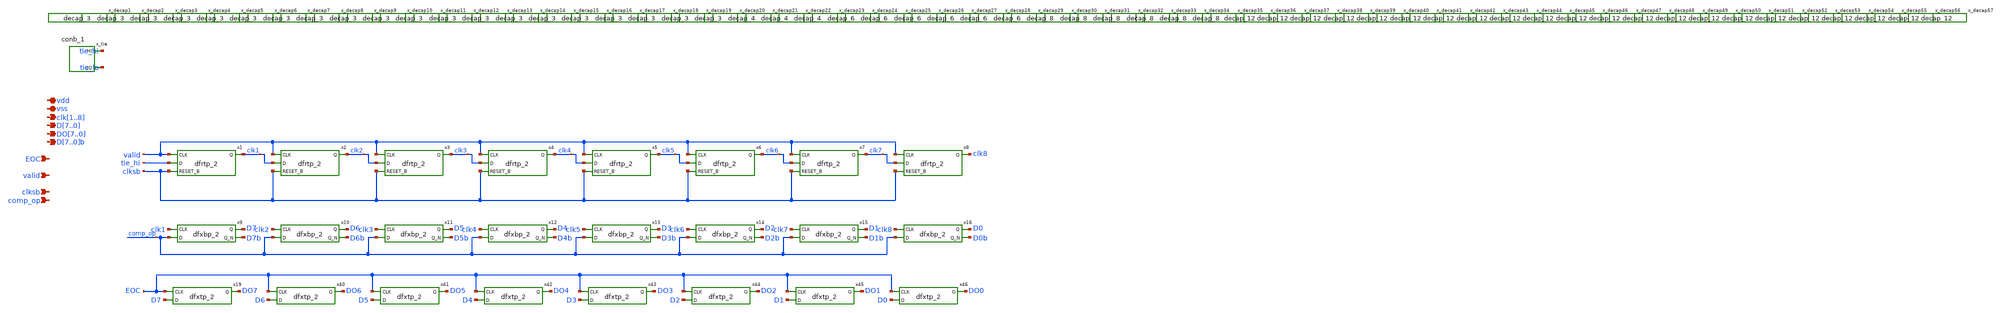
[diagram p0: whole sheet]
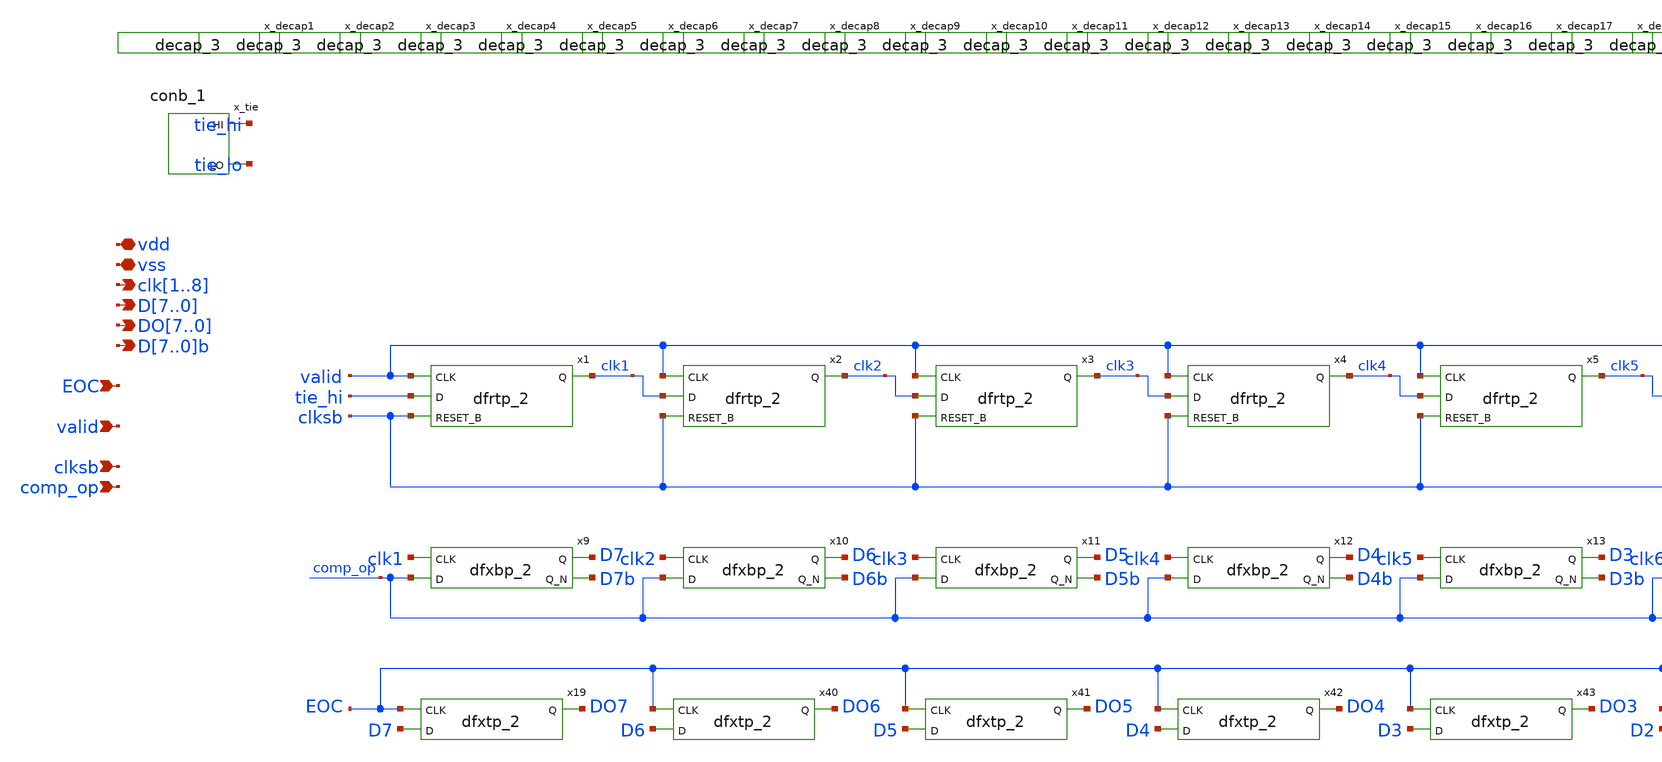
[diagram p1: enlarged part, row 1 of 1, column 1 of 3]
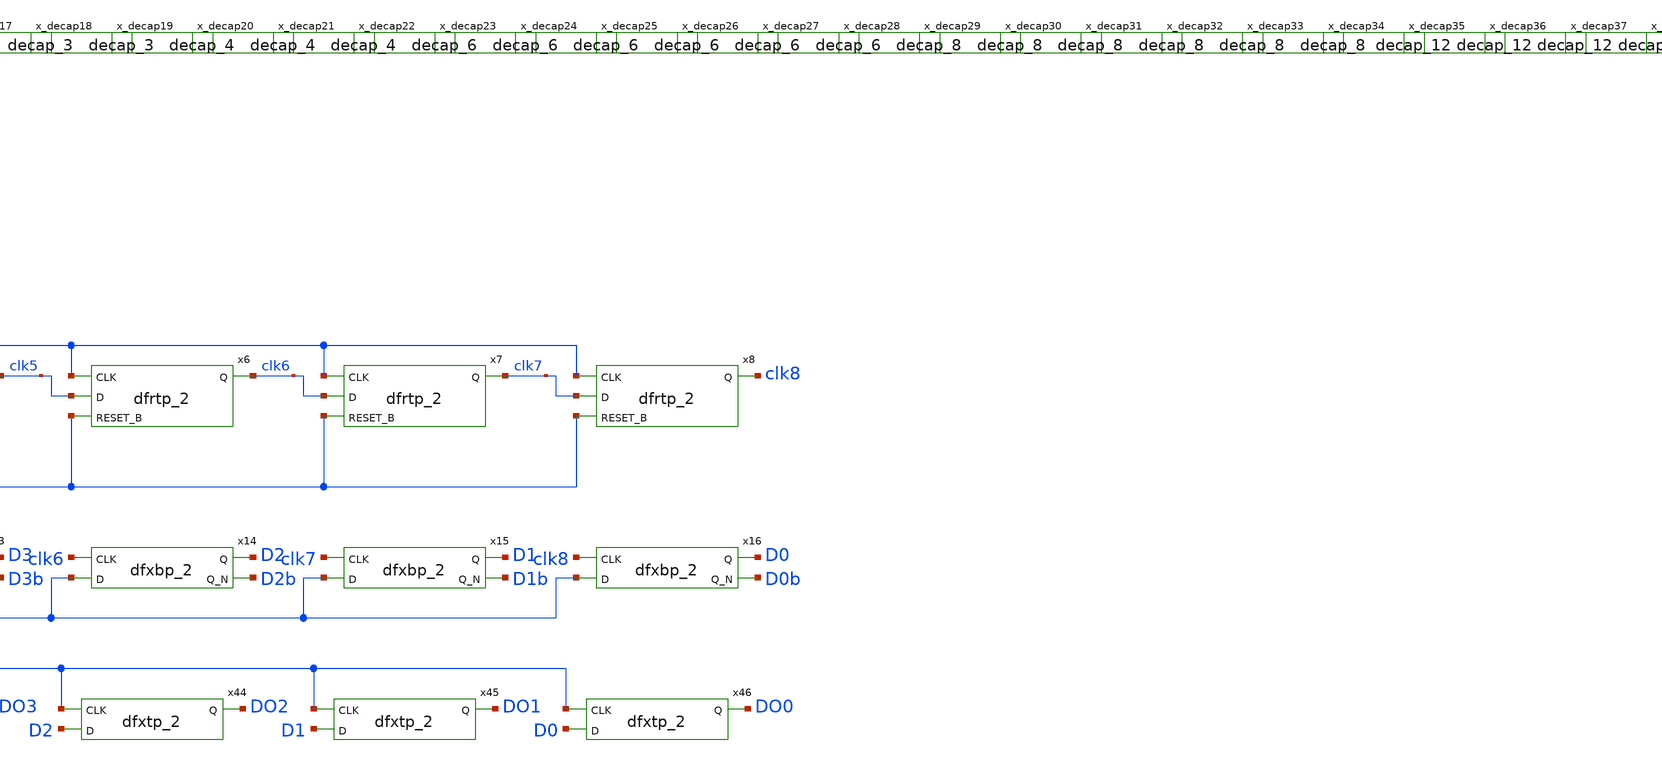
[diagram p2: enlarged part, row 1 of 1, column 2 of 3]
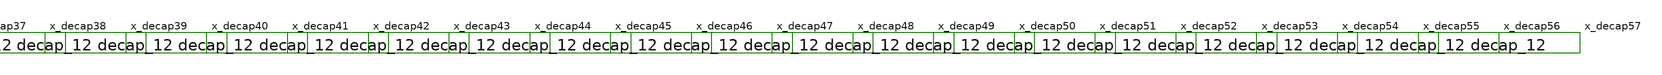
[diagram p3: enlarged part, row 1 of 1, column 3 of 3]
** sch_path: xschem/sar-adc/sarlogic.sch
**.subckt sarlogic valid comp_op D7,D6,D5,D4,D3,D2,D1,D0 vdd vss D7b,D6b,D5b,D4b,D3b,D2b,D1b,D0b
*+ clk1,clk2,clk3,clk4,clk5,clk6,clk7,clk8 DO7,DO6,DO5,DO4,DO3,DO2,DO1,DO0 clksb EOC
*.ipin valid
*.ipin comp_op
*.opin D7,D6,D5,D4,D3,D2,D1,D0
*.iopin vdd
*.iopin vss
*.opin D7b,D6b,D5b,D4b,D3b,D2b,D1b,D0b
*.opin clk1,clk2,clk3,clk4,clk5,clk6,clk7,clk8
*.opin DO7,DO6,DO5,DO4,DO3,DO2,DO1,DO0
*.ipin clksb
*.ipin EOC
x1 valid tie_hi clksb vss vss vdd vdd clk1 sky130_fd_sc_hd__dfrtp_2
x2 valid clk1 clksb vss vss vdd vdd clk2 sky130_fd_sc_hd__dfrtp_2
x3 valid clk2 clksb vss vss vdd vdd clk3 sky130_fd_sc_hd__dfrtp_2
x4 valid clk3 clksb vss vss vdd vdd clk4 sky130_fd_sc_hd__dfrtp_2
x5 valid clk4 clksb vss vss vdd vdd clk5 sky130_fd_sc_hd__dfrtp_2
x6 valid clk5 clksb vss vss vdd vdd clk6 sky130_fd_sc_hd__dfrtp_2
x7 valid clk6 clksb vss vss vdd vdd clk7 sky130_fd_sc_hd__dfrtp_2
x8 valid clk7 clksb vss vss vdd vdd clk8 sky130_fd_sc_hd__dfrtp_2
x19 EOC D7 vss vss vdd vdd DO7 sky130_fd_sc_hd__dfxtp_2
x40 EOC D6 vss vss vdd vdd DO6 sky130_fd_sc_hd__dfxtp_2
x41 EOC D5 vss vss vdd vdd DO5 sky130_fd_sc_hd__dfxtp_2
x42 EOC D4 vss vss vdd vdd DO4 sky130_fd_sc_hd__dfxtp_2
x43 EOC D3 vss vss vdd vdd DO3 sky130_fd_sc_hd__dfxtp_2
x44 EOC D2 vss vss vdd vdd DO2 sky130_fd_sc_hd__dfxtp_2
x45 EOC D1 vss vss vdd vdd DO1 sky130_fd_sc_hd__dfxtp_2
x46 EOC D0 vss vss vdd vdd DO0 sky130_fd_sc_hd__dfxtp_2
x9 clk1 comp_op vss vss vdd vdd D7 D7b sky130_fd_sc_hd__dfxbp_2
x10 clk2 comp_op vss vss vdd vdd D6 D6b sky130_fd_sc_hd__dfxbp_2
x11 clk3 comp_op vss vss vdd vdd D5 D5b sky130_fd_sc_hd__dfxbp_2
x12 clk4 comp_op vss vss vdd vdd D4 D4b sky130_fd_sc_hd__dfxbp_2
x13 clk5 comp_op vss vss vdd vdd D3 D3b sky130_fd_sc_hd__dfxbp_2
x14 clk6 comp_op vss vss vdd vdd D2 D2b sky130_fd_sc_hd__dfxbp_2
x15 clk7 comp_op vss vss vdd vdd D1 D1b sky130_fd_sc_hd__dfxbp_2
x16 clk8 comp_op vss vss vdd vdd D0 D0b sky130_fd_sc_hd__dfxbp_2
x_tie vss vss vdd vdd tie_hi tie_lo sky130_fd_sc_hd__conb_1
x_decap1 vss vss vdd vdd sky130_fd_sc_hd__decap_3
x_decap2 vss vss vdd vdd sky130_fd_sc_hd__decap_3
x_decap3 vss vss vdd vdd sky130_fd_sc_hd__decap_3
x_decap4 vss vss vdd vdd sky130_fd_sc_hd__decap_3
x_decap5 vss vss vdd vdd sky130_fd_sc_hd__decap_3
x_decap6 vss vss vdd vdd sky130_fd_sc_hd__decap_3
x_decap7 vss vss vdd vdd sky130_fd_sc_hd__decap_3
x_decap8 vss vss vdd vdd sky130_fd_sc_hd__decap_3
x_decap9 vss vss vdd vdd sky130_fd_sc_hd__decap_3
x_decap10 vss vss vdd vdd sky130_fd_sc_hd__decap_3
x_decap11 vss vss vdd vdd sky130_fd_sc_hd__decap_3
x_decap12 vss vss vdd vdd sky130_fd_sc_hd__decap_3
x_decap13 vss vss vdd vdd sky130_fd_sc_hd__decap_3
x_decap14 vss vss vdd vdd sky130_fd_sc_hd__decap_3
x_decap15 vss vss vdd vdd sky130_fd_sc_hd__decap_3
x_decap16 vss vss vdd vdd sky130_fd_sc_hd__decap_3
x_decap17 vss vss vdd vdd sky130_fd_sc_hd__decap_3
x_decap18 vss vss vdd vdd sky130_fd_sc_hd__decap_3
x_decap19 vss vss vdd vdd sky130_fd_sc_hd__decap_3
x_decap20 vss vss vdd vdd sky130_fd_sc_hd__decap_3
x_decap21 vss vss vdd vdd sky130_fd_sc_hd__decap_4
x_decap22 vss vss vdd vdd sky130_fd_sc_hd__decap_4
x_decap23 vss vss vdd vdd sky130_fd_sc_hd__decap_4
x_decap24 vss vss vdd vdd sky130_fd_sc_hd__decap_6
x_decap25 vss vss vdd vdd sky130_fd_sc_hd__decap_6
x_decap26 vss vss vdd vdd sky130_fd_sc_hd__decap_6
x_decap27 vss vss vdd vdd sky130_fd_sc_hd__decap_6
x_decap28 vss vss vdd vdd sky130_fd_sc_hd__decap_6
x_decap29 vss vss vdd vdd sky130_fd_sc_hd__decap_6
x_decap30 vss vss vdd vdd sky130_fd_sc_hd__decap_8
x_decap31 vss vss vdd vdd sky130_fd_sc_hd__decap_8
x_decap32 vss vss vdd vdd sky130_fd_sc_hd__decap_8
x_decap33 vss vss vdd vdd sky130_fd_sc_hd__decap_8
x_decap34 vss vss vdd vdd sky130_fd_sc_hd__decap_8
x_decap35 vss vss vdd vdd sky130_fd_sc_hd__decap_8
x_decap36 vss vss vdd vdd sky130_fd_sc_hd__decap_12
x_decap37 vss vss vdd vdd sky130_fd_sc_hd__decap_12
x_decap38 vss vss vdd vdd sky130_fd_sc_hd__decap_12
x_decap39 vss vss vdd vdd sky130_fd_sc_hd__decap_12
x_decap40 vss vss vdd vdd sky130_fd_sc_hd__decap_12
x_decap41 vss vss vdd vdd sky130_fd_sc_hd__decap_12
x_decap42 vss vss vdd vdd sky130_fd_sc_hd__decap_12
x_decap43 vss vss vdd vdd sky130_fd_sc_hd__decap_12
x_decap44 vss vss vdd vdd sky130_fd_sc_hd__decap_12
x_decap45 vss vss vdd vdd sky130_fd_sc_hd__decap_12
x_decap46 vss vss vdd vdd sky130_fd_sc_hd__decap_12
x_decap47 vss vss vdd vdd sky130_fd_sc_hd__decap_12
x_decap48 vss vss vdd vdd sky130_fd_sc_hd__decap_12
x_decap49 vss vss vdd vdd sky130_fd_sc_hd__decap_12
x_decap50 vss vss vdd vdd sky130_fd_sc_hd__decap_12
x_decap51 vss vss vdd vdd sky130_fd_sc_hd__decap_12
x_decap52 vss vss vdd vdd sky130_fd_sc_hd__decap_12
x_decap53 vss vss vdd vdd sky130_fd_sc_hd__decap_12
x_decap54 vss vss vdd vdd sky130_fd_sc_hd__decap_12
x_decap55 vss vss vdd vdd sky130_fd_sc_hd__decap_12
x_decap56 vss vss vdd vdd sky130_fd_sc_hd__decap_12
x_decap57 vss vss vdd vdd sky130_fd_sc_hd__decap_12
**.ends
.end
